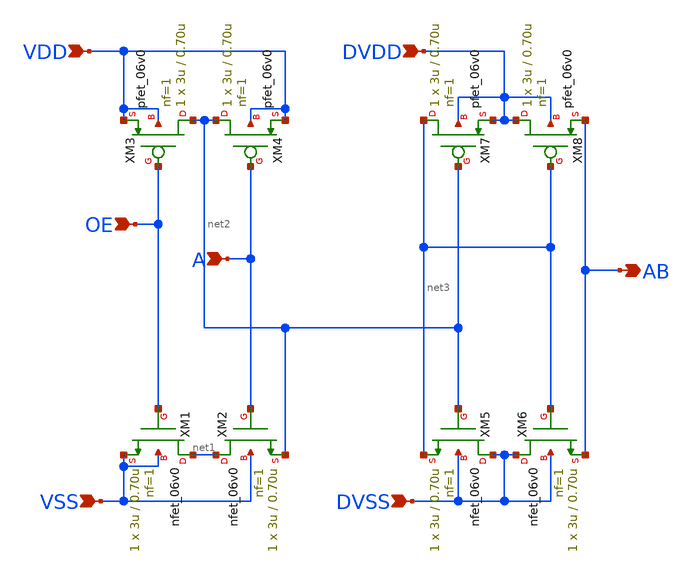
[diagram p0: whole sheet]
** sch_path: gf180mcu_fd_io__bi_24t/comp018green_out_sigbuf_a.sch
**.subckt comp018green_out_sigbuf_a OE A VDD VSS DVSS DVDD AB
*.ipin OE
*.ipin A
*.ipin VDD
*.ipin VSS
*.ipin DVSS
*.ipin DVDD
*.opin AB
XM1 net1 OE VSS VSS nfet_06v0 L=0.70u W=3u nf=1 ad='int((nf+1)/2) * W/nf * 0.18u' as='int((nf+2)/2) * W/nf * 0.18u'
+ pd='2*int((nf+1)/2) * (W/nf + 0.18u)' ps='2*int((nf+2)/2) * (W/nf + 0.18u)' nrd='0.18u / W' nrs='0.18u / W'
+ sa=0 sb=0 sd=0 m=1
XM2 net1 A net2 VSS nfet_06v0 L=0.70u W=3u nf=1 ad='int((nf+1)/2) * W/nf * 0.18u' as='int((nf+2)/2) * W/nf * 0.18u'
+ pd='2*int((nf+1)/2) * (W/nf + 0.18u)' ps='2*int((nf+2)/2) * (W/nf + 0.18u)' nrd='0.18u / W' nrs='0.18u / W'
+ sa=0 sb=0 sd=0 m=1
XM3 net2 OE VDD VDD pfet_06v0 L=0.70u W=3u nf=1 ad='int((nf+1)/2) * W/nf * 0.18u' as='int((nf+2)/2) * W/nf * 0.18u'
+ pd='2*int((nf+1)/2) * (W/nf + 0.18u)' ps='2*int((nf+2)/2) * (W/nf + 0.18u)' nrd='0.18u / W' nrs='0.18u / W'
+ sa=0 sb=0 sd=0 m=1
XM4 net2 A VDD VDD pfet_06v0 L=0.70u W=3u nf=1 ad='int((nf+1)/2) * W/nf * 0.18u' as='int((nf+2)/2) * W/nf * 0.18u'
+ pd='2*int((nf+1)/2) * (W/nf + 0.18u)' ps='2*int((nf+2)/2) * (W/nf + 0.18u)' nrd='0.18u / W' nrs='0.18u / W'
+ sa=0 sb=0 sd=0 m=1
XM5 DVSS net2 net3 DVSS nfet_06v0 L=0.70u W=3u nf=1 ad='int((nf+1)/2) * W/nf * 0.18u' as='int((nf+2)/2) * W/nf * 0.18u'
+ pd='2*int((nf+1)/2) * (W/nf + 0.18u)' ps='2*int((nf+2)/2) * (W/nf + 0.18u)' nrd='0.18u / W' nrs='0.18u / W'
+ sa=0 sb=0 sd=0 m=1
XM6 DVSS net3 AB DVSS nfet_06v0 L=0.70u W=3u nf=1 ad='int((nf+1)/2) * W/nf * 0.18u' as='int((nf+2)/2) * W/nf * 0.18u'
+ pd='2*int((nf+1)/2) * (W/nf + 0.18u)' ps='2*int((nf+2)/2) * (W/nf + 0.18u)' nrd='0.18u / W' nrs='0.18u / W'
+ sa=0 sb=0 sd=0 m=1
XM7 net3 net2 DVDD DVDD pfet_06v0 L=0.70u W=3u nf=1 ad='int((nf+1)/2) * W/nf * 0.18u' as='int((nf+2)/2) * W/nf * 0.18u'
+ pd='2*int((nf+1)/2) * (W/nf + 0.18u)' ps='2*int((nf+2)/2) * (W/nf + 0.18u)' nrd='0.18u / W' nrs='0.18u / W'
+ sa=0 sb=0 sd=0 m=1
XM8 DVDD net3 AB DVDD pfet_06v0 L=0.70u W=3u nf=1 ad='int((nf+1)/2) * W/nf * 0.18u' as='int((nf+2)/2) * W/nf * 0.18u'
+ pd='2*int((nf+1)/2) * (W/nf + 0.18u)' ps='2*int((nf+2)/2) * (W/nf + 0.18u)' nrd='0.18u / W' nrs='0.18u / W'
+ sa=0 sb=0 sd=0 m=1
**.ends
.end
